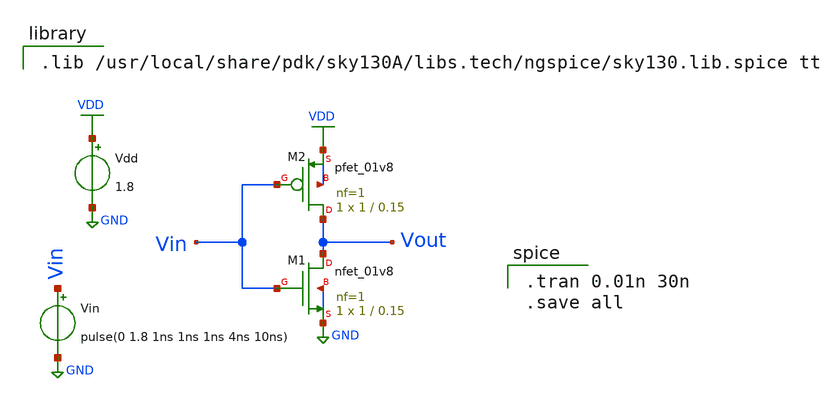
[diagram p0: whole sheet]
** sch_path: Week-1/Inverter_Pre-Layout/inverter.sch
**.subckt inverter
XM1 Vout Vin GND GND sky130_fd_pr__nfet_01v8 L=0.15 W=1 nf=1 ad='int((nf+1)/2) * W/nf * 0.29' as='int((nf+2)/2) * W/nf * 0.29'
+ pd='2*int((nf+1)/2) * (W/nf + 0.29)' ps='2*int((nf+2)/2) * (W/nf + 0.29)' nrd='0.29 / W' nrs='0.29 / W'
+ sa=0 sb=0 sd=0 mult=1 m=1
XM2 Vout Vin VDD VDD sky130_fd_pr__pfet_01v8 L=0.15 W=1 nf=1 ad='int((nf+1)/2) * W/nf * 0.29' as='int((nf+2)/2) * W/nf * 0.29'
+ pd='2*int((nf+1)/2) * (W/nf + 0.29)' ps='2*int((nf+2)/2) * (W/nf + 0.29)' nrd='0.29 / W' nrs='0.29 / W'
+ sa=0 sb=0 sd=0 mult=1 m=1
Vdd VDD GND 1.8
Vin Vin GND pulse(0 1.8 1ns 1ns 1ns 4ns 10ns)
**** begin user architecture code

.tran 0.01n 30n
.save all


.lib /usr/local/share/pdk/sky130A/libs.tech/ngspice/sky130.lib.spice tt

**** end user architecture code
**.ends
.GLOBAL GND
.GLOBAL VDD
.end
